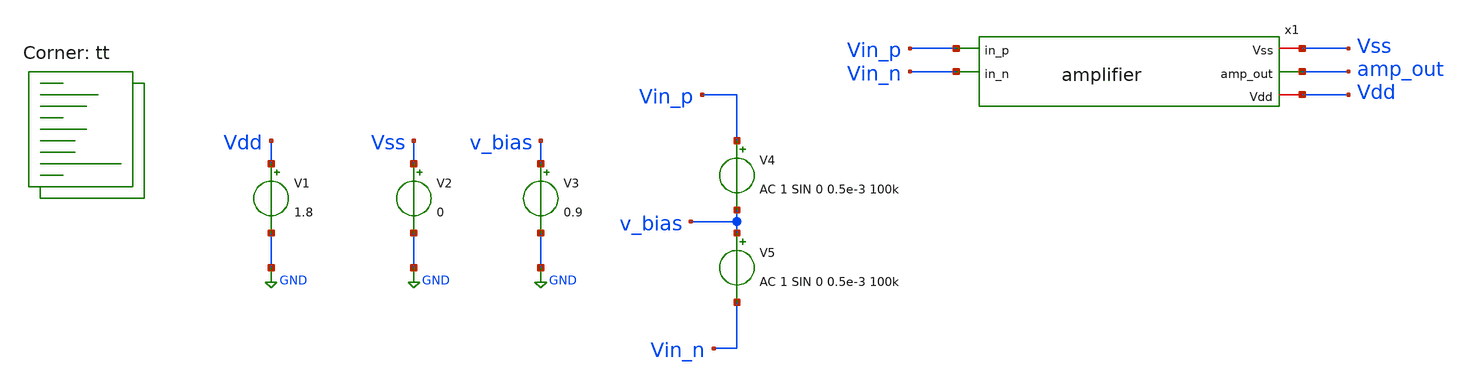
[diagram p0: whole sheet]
** sch_path: xschem/tests/amp_sim.sch
**.subckt amp_sim
V1 Vdd GND 1.8
V2 Vss GND 0
V3 v_bias GND 0.9
V4 Vin_p v_bias AC 1 SIN 0 0.5e-3 100k
V5 v_bias Vin_n AC 1 SIN 0 0.5e-3 100k
x1 Vss amp_out Vdd Vin_p Vin_n amplifier
**** begin user architecture code
.lib $::SKYWATER_MODELS/sky130.lib.spice tt


* ngspice commands
.options method = gear
.control
save all
ac dec 10 10 1e9
*tran 0.1u 100u 0
.endc



**** end user architecture code
**.ends
.GLOBAL GND
.end
